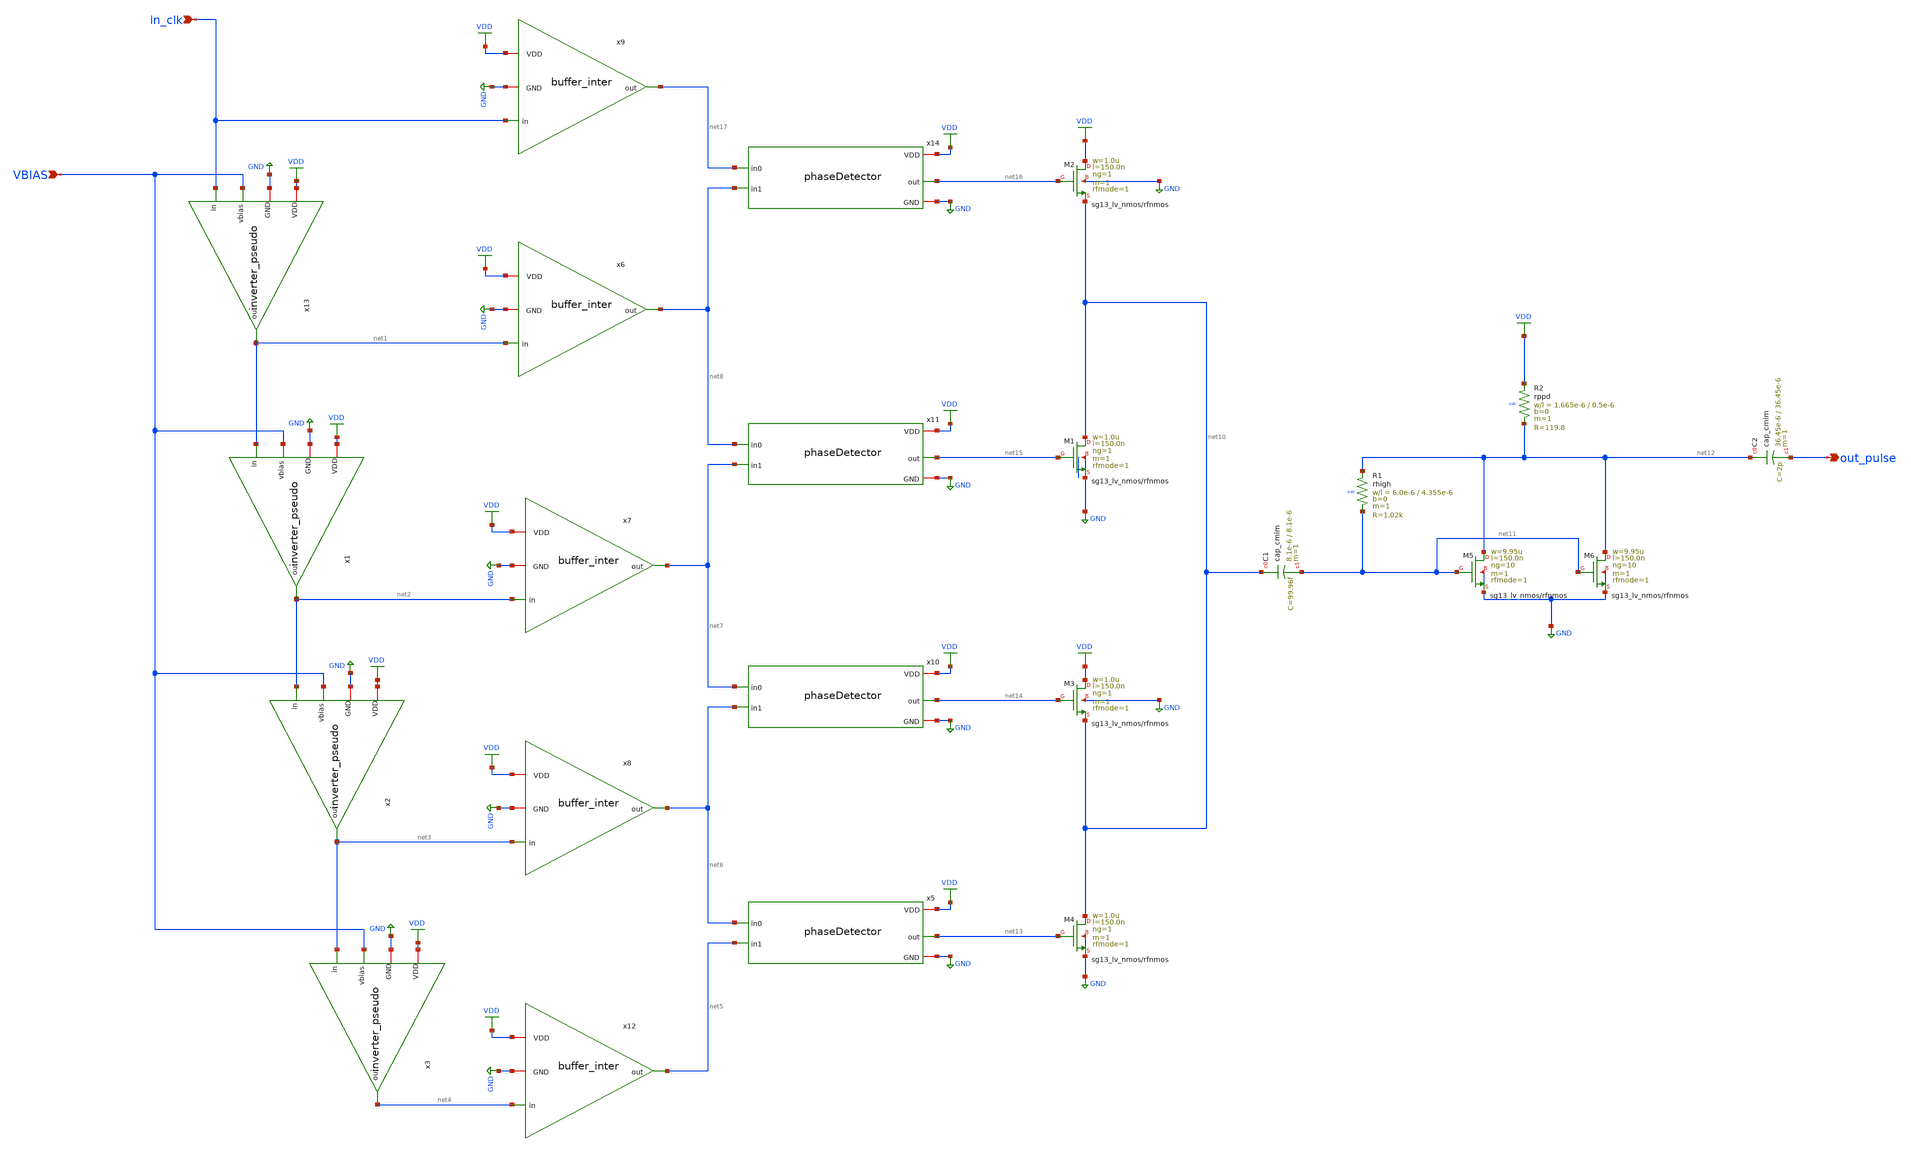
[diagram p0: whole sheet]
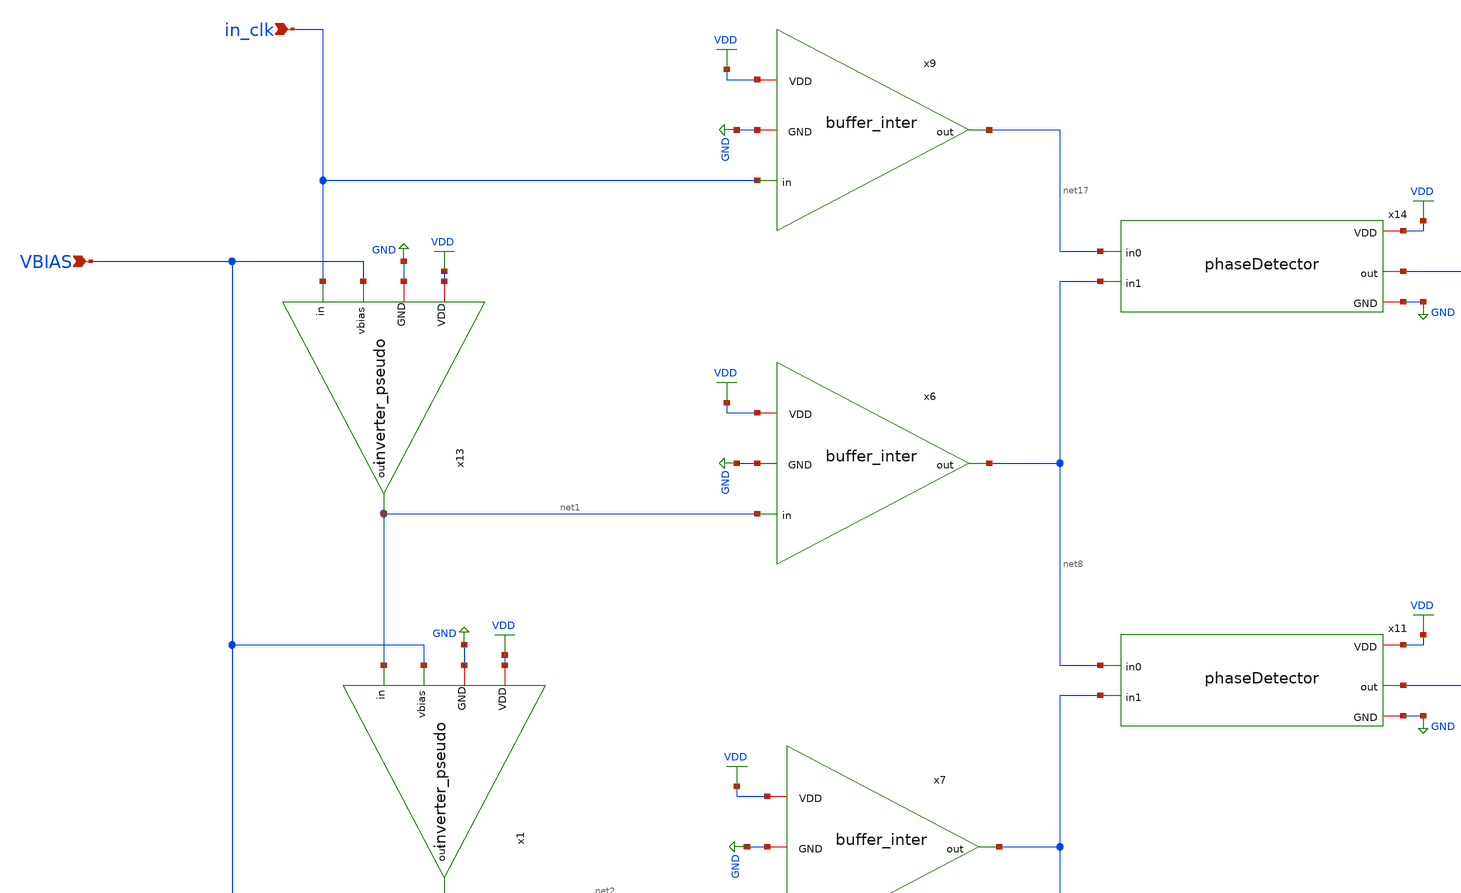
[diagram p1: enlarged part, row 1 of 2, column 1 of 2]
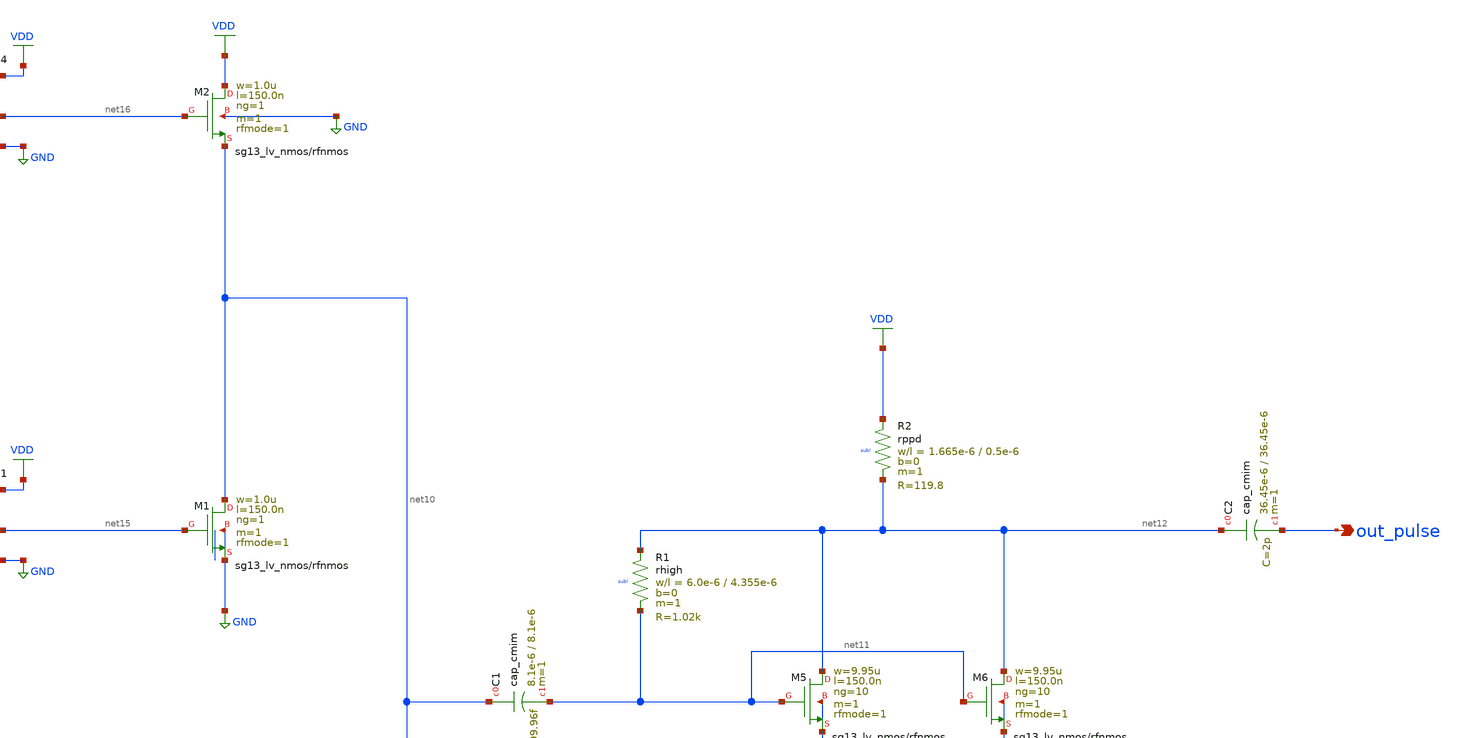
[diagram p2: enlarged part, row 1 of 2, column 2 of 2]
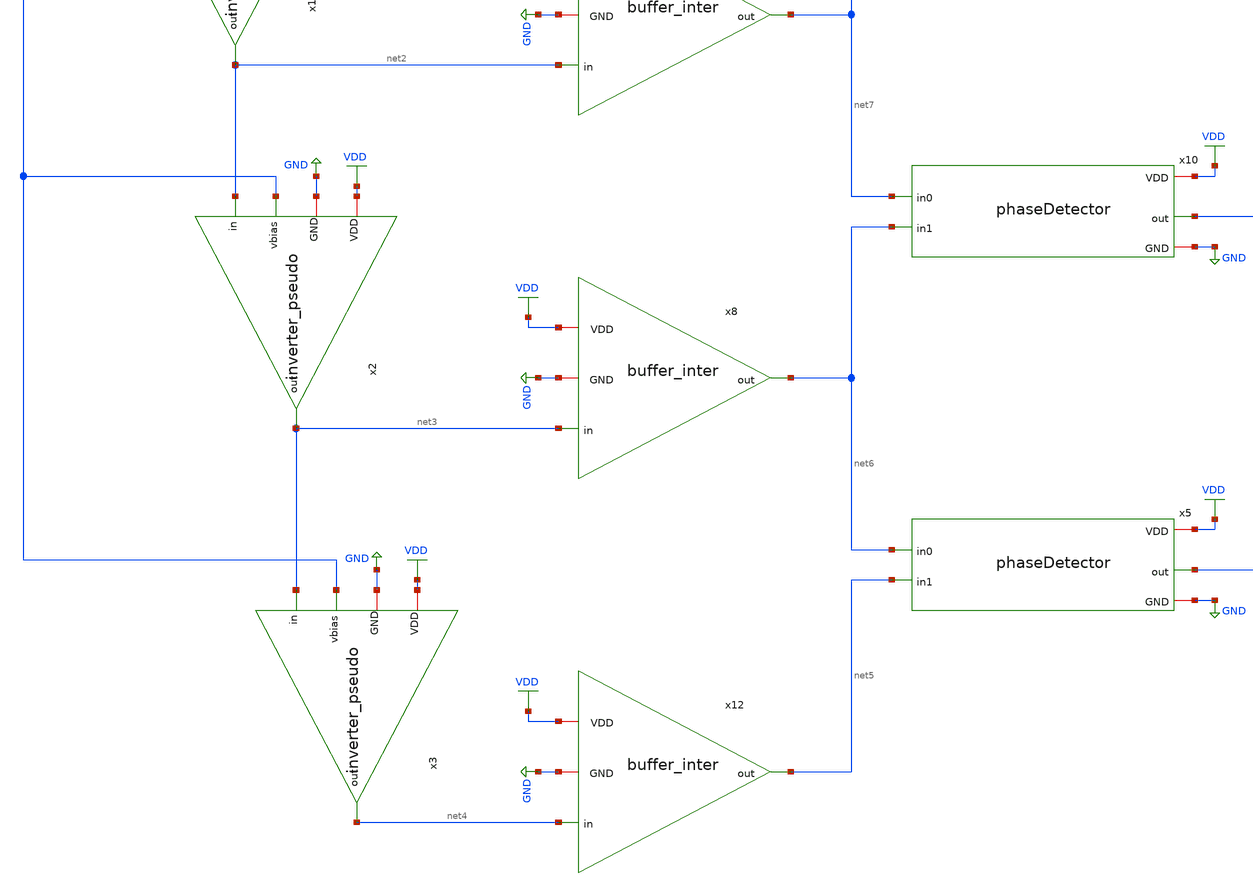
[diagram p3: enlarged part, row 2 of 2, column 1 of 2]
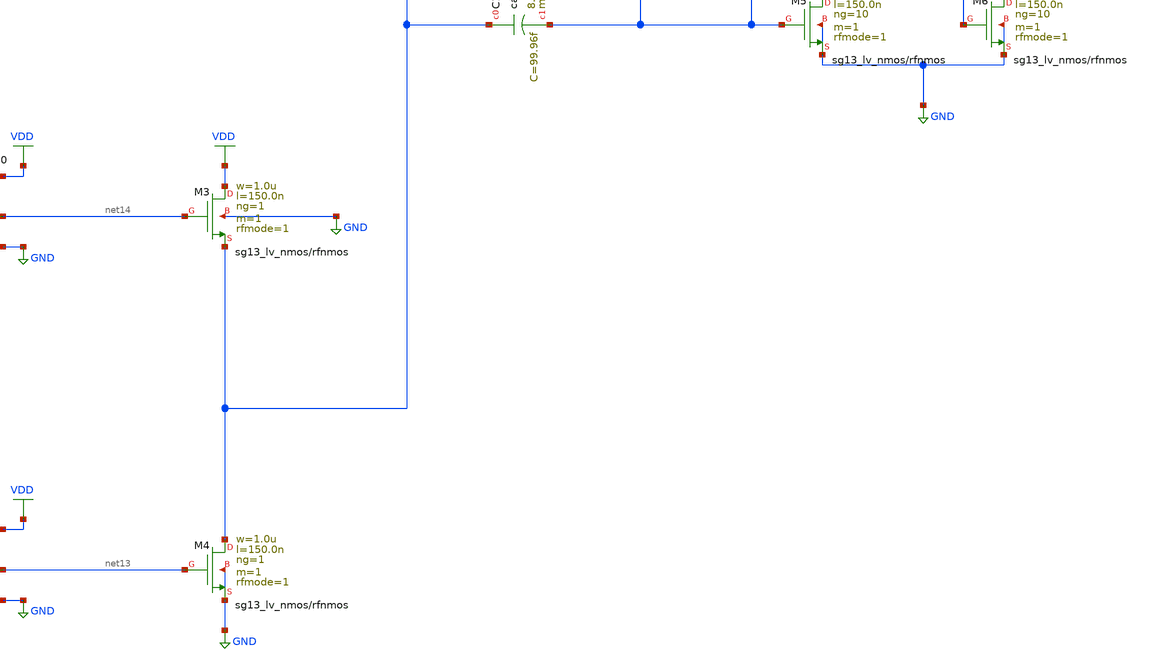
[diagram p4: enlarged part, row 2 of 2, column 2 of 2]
** sch_path: UWBPulseGenerator/design_data/xschem/uwbPG.sch
**.subckt uwbPG VBIAS in_clk out_pulse
*.ipin VBIAS
*.ipin in_clk
*.opin out_pulse
XM1 net10 net15 GND GND sg13_lv_nmos w=1.0u l=150.0n ng=1 m=1 rfmode=1 mm_ok=1
XM3 VDD net14 net10 GND sg13_lv_nmos w=1.0u l=150.0n ng=1 m=1 rfmode=1 mm_ok=1
XM4 net10 net13 GND GND sg13_lv_nmos w=1.0u l=150.0n ng=1 m=1 rfmode=1 mm_ok=1
XC1 net10 net11 cap_cmim w=8.1e-6 l=8.1e-6 m=1 mm_ok=1
XM5 net12 net11 GND GND sg13_lv_nmos w=9.95u l=150.0n ng=10 m=1 rfmode=1 mm_ok=1
XM6 net12 net11 GND GND sg13_lv_nmos w=9.95u l=150.0n ng=10 m=1 rfmode=1 mm_ok=1
XR1 net12 net11 sub! rhigh w=6.0e-6 l=4.355e-6 m=1 b=0 mm_ok=1
XR2 VDD net12 sub! rppd w=1.665e-6 l=0.5e-6 m=1 b=0 mm_ok=1
XC2 net12 out_pulse cap_cmim w=36.45e-6 l=36.45e-6 m=1 mm_ok=1
XM2 VDD net16 net10 GND sg13_lv_nmos w=1.0u l=150.0n ng=1 m=1 rfmode=1 mm_ok=1
x14 VDD net16 net17 net8 GND phaseDetector
x11 VDD net15 net8 net7 GND phaseDetector
x10 VDD net14 net7 net6 GND phaseDetector
x5 VDD net13 net6 net5 GND phaseDetector
x12 VDD net4 net5 GND buffer_inter
x8 VDD net3 net6 GND buffer_inter
x7 VDD net2 net7 GND buffer_inter
x6 VDD net1 net8 GND buffer_inter
x9 VDD in_clk net17 GND buffer_inter
x13 VDD VBIAS net1 in_clk GND inverter_pseudo
x1 VDD VBIAS net2 net1 GND inverter_pseudo
x2 VDD VBIAS net3 net2 GND inverter_pseudo
x3 VDD VBIAS net4 net3 GND inverter_pseudo
**.ends

* expanding   symbol:  /foss/designs/reklayoutgeradordepulso/phaseDetector.sym # of pins=5
** sym_path: UWBPulseGenerator/design_data/xschem/phaseDetector.sym
** sch_path: UWBPulseGenerator/design_data/xschem/phaseDetector.sch
.subckt phaseDetector VDD out in0 in1 GND
*.ipin in0
*.ipin in1
*.opin out
*.iopin GND
*.iopin VDD
XM2 net1 in0 GND GND sg13_lv_nmos w=500.0n l=150.0n ng=1 m=1 rfmode=1 mm_ok=1
XM1 net2 in1 net1 GND sg13_lv_nmos w=500.0n l=150.0n ng=1 m=1 rfmode=1 mm_ok=1
XM3 net2 in0 VDD VDD sg13_lv_pmos w=1.5u l=150.0n ng=1 m=1 rfmode=1 mm_ok=1
XM4 net4 net2 VDD VDD sg13_lv_pmos w=1.5u l=150.0n ng=1 m=1 rfmode=1 mm_ok=1
XM5 out net4 VDD VDD sg13_lv_pmos w=1.5u l=150.0n ng=1 m=1 rfmode=1 mm_ok=1
XM6 net3 in0 GND GND sg13_lv_nmos w=500.0n l=150.0n ng=1 m=1 rfmode=1 mm_ok=1
XM7 net4 net2 net3 GND sg13_lv_nmos w=500.0n l=150.0n ng=1 m=1 rfmode=1 mm_ok=1
XM9 out net4 GND GND sg13_lv_nmos w=500.0n l=150.0n ng=1 m=1 rfmode=1 mm_ok=1
.ends


* expanding   symbol:  /foss/designs/reklayoutgeradordepulso/buffer_inter.sym # of pins=4
** sym_path: UWBPulseGenerator/design_data/xschem/buffer_inter.sym
** sch_path: UWBPulseGenerator/design_data/xschem/buffer_inter.sch
.subckt buffer_inter VDD in out GND
*.ipin in
*.opin out
*.iopin VDD
*.iopin GND
XM1 net1 in GND GND sg13_lv_nmos w=500.0n l=150.0n ng=1 m=1 rfmode=1 mm_ok=1
XM3 net1 in VDD VDD sg13_lv_pmos w=1.0u l=150.0n ng=1 m=1 rfmode=1 mm_ok=1
XM2 net2 net1 GND GND sg13_lv_nmos w=1.0u l=150.0n ng=1 m=1 rfmode=1 mm_ok=1
XM4 net2 net1 VDD VDD sg13_lv_pmos w=2.0u l=150.0n ng=1 m=1 rfmode=1 mm_ok=1
XM5 net3 net2 GND GND sg13_lv_nmos w=500.0n l=150.0n ng=1 m=1 rfmode=1 mm_ok=1
XM6 net3 net2 VDD VDD sg13_lv_pmos w=1.0u l=150.0n ng=1 m=1 rfmode=1 mm_ok=1
XM7 out net3 GND GND sg13_lv_nmos w=1.0u l=150.0n ng=1 m=1 rfmode=1 mm_ok=1
XM8 out net3 VDD VDD sg13_lv_pmos w=2.0u l=150.0n ng=1 m=1 rfmode=1 mm_ok=1
.ends


* expanding   symbol:  /foss/designs/reklayoutgeradordepulso/inverter_pseudo.sym # of pins=5
** sym_path: UWBPulseGenerator/design_data/xschem/inverter_pseudo.sym
** sch_path: UWBPulseGenerator/design_data/xschem/inverter_pseudo.sch
.subckt inverter_pseudo VDD vbias out in GND
*.ipin vbias
*.ipin in
*.opin out
*.iopin VDD
*.iopin GND
XM1 net1 in GND GND sg13_lv_nmos w=500.0n l=150.0n ng=1 m=1 rfmode=1 mm_ok=1
XM3 net1 vbias VDD VDD sg13_lv_pmos w=1.7u l=150.0n ng=1 m=1 rfmode=1 mm_ok=1
XM2 out net1 GND GND sg13_lv_nmos w=500.0n l=150.0n ng=1 m=1 rfmode=1 mm_ok=1
XM4 out vbias VDD VDD sg13_lv_pmos w=1.7u l=150.0n ng=1 m=1 rfmode=1 mm_ok=1
.ends

.GLOBAL GND
.GLOBAL VDD
.end
